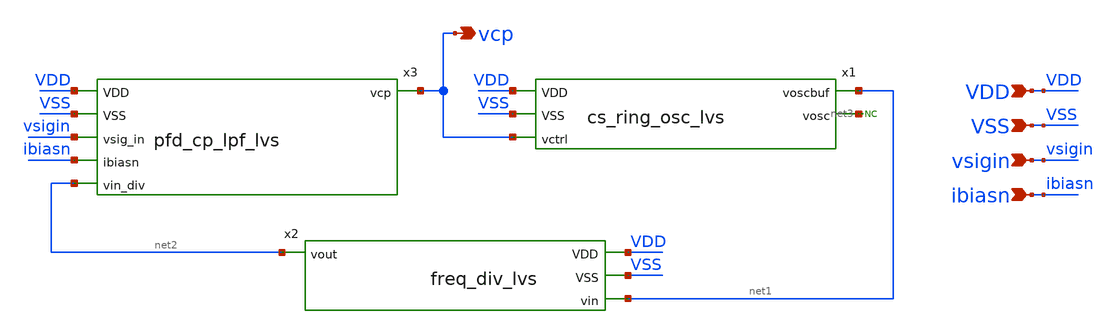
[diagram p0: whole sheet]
** sch_path: designs/low_freq_pll_block_lvs.sch
**.subckt low_freq_pll_block_lvs VDD VSS vsigin ibiasn vcp
*.ipin VDD
*.ipin VSS
*.ipin vsigin
*.ipin ibiasn
*.opin vcp
x1 VDD VSS net1 net3 vcp cs_ring_osc_lvs
x2 VDD VSS net1 net2 freq_div_lvs
x3 VDD VSS vsigin ibiasn vcp net2 pfd_cp_lpf_lvs
* noconn #net3
**.ends
.end
